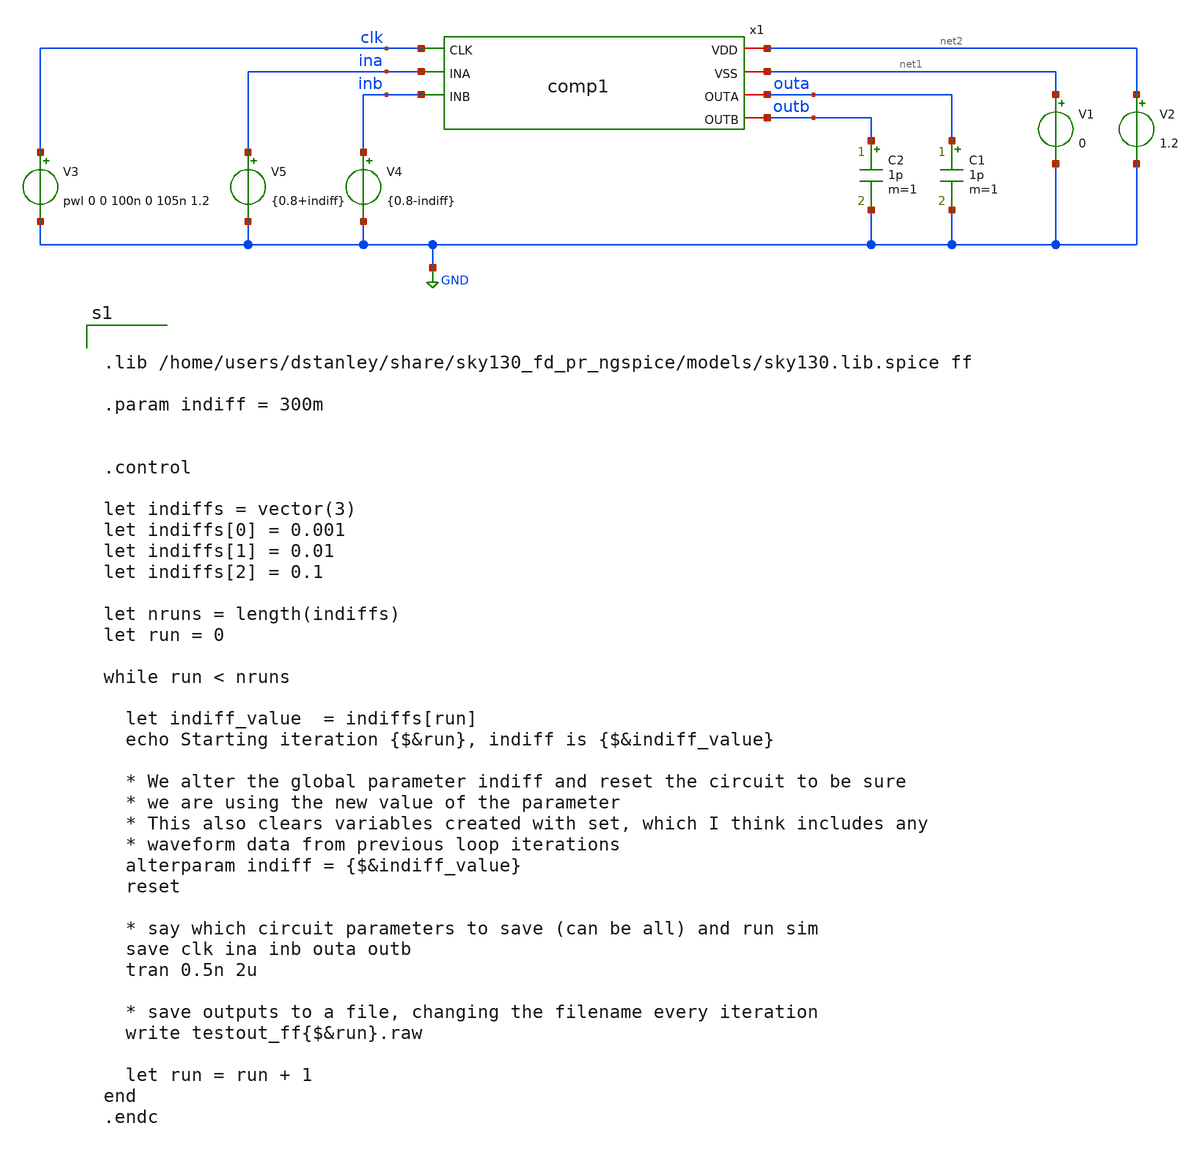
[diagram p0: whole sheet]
** sch_path: comp1_loop_test_ff.sch
**.subckt comp1_loop_test_ff
x1 net2 net1 clk ina inb outa outb comp1
V1 net1 GND 0
V2 net2 GND 1.2
C1 outa GND 1p m=1
C2 outb GND 1p m=1
V3 clk GND pwl 0 0 100n 0 105n 1.2
V4 inb GND {0.8-indiff}
V5 ina GND {0.8+indiff}
**** begin user architecture code


.lib /home/users/dstanley/share/sky130_fd_pr_ngspice/models/sky130.lib.spice ff

.param indiff = 300m


.control

let indiffs = vector(3)
let indiffs[0] = 0.001
let indiffs[1] = 0.01
let indiffs[2] = 0.1

let nruns = length(indiffs)
let run = 0

while run < nruns

  let indiff_value  = indiffs[run]
  echo Starting iteration {$&run}, indiff is {$&indiff_value}

  * We alter the global parameter indiff and reset the circuit to be sure
  * we are using the new value of the parameter
  * This also clears variables created with set, which I think includes any
  * waveform data from previous loop iterations
  alterparam indiff = {$&indiff_value}
  reset

  * say which circuit parameters to save (can be all) and run sim
  save clk ina inb outa outb
  tran 0.5n 2u

  * save outputs to a file, changing the filename every iteration
  write testout_ff{$&run}.raw

  let run = run + 1
end
.endc


**** end user architecture code
**.ends

* expanding   symbol:  /home/users/dstanley/EE272B/xschem_tests/comp1.sym # of pins=7
** sym_path: comp1.sym
** sch_path: comp1.sch
.subckt comp1 VDD VSS CLK INA INB OUTA OUTB
*.iopin VSS
*.iopin VDD
*.iopin OUTB
*.iopin OUTA
*.ipin INB
*.ipin INA
*.ipin CLK
XM1 net2 CLK VSS VSS sky130_fd_pr__nfet_01v8 L=0.15 W=1 nf=1 ad='int((nf+1)/2) * W/nf * 0.29' as='int((nf+2)/2) * W/nf * 0.29'
+ pd='2*int((nf+1)/2) * (W/nf + 0.29)' ps='2*int((nf+2)/2) * (W/nf + 0.29)' nrd='0.29 / W' nrs='0.29 / W'
+ sa=0 sb=0 sd=0 mult=1 m=1
XM2 net1 INA net2 VSS sky130_fd_pr__nfet_01v8 L=0.15 W=1 nf=1 ad='int((nf+1)/2) * W/nf * 0.29' as='int((nf+2)/2) * W/nf * 0.29'
+ pd='2*int((nf+1)/2) * (W/nf + 0.29)' ps='2*int((nf+2)/2) * (W/nf + 0.29)' nrd='0.29 / W' nrs='0.29 / W'
+ sa=0 sb=0 sd=0 mult=1 m=1
XM4 OUTB OUTA net1 VSS sky130_fd_pr__nfet_01v8 L=0.15 W=1 nf=1 ad='int((nf+1)/2) * W/nf * 0.29' as='int((nf+2)/2) * W/nf * 0.29'
+ pd='2*int((nf+1)/2) * (W/nf + 0.29)' ps='2*int((nf+2)/2) * (W/nf + 0.29)' nrd='0.29 / W' nrs='0.29 / W'
+ sa=0 sb=0 sd=0 mult=1 m=1
XM5 OUTB OUTA VDD VDD sky130_fd_pr__pfet_01v8 L=0.15 W=1 nf=1 ad='int((nf+1)/2) * W/nf * 0.29' as='int((nf+2)/2) * W/nf * 0.29'
+ pd='2*int((nf+1)/2) * (W/nf + 0.29)' ps='2*int((nf+2)/2) * (W/nf + 0.29)' nrd='0.29 / W' nrs='0.29 / W'
+ sa=0 sb=0 sd=0 mult=1 m=1
XM6 OUTB CLK VDD VDD sky130_fd_pr__pfet_01v8 L=0.15 W=1 nf=1 ad='int((nf+1)/2) * W/nf * 0.29' as='int((nf+2)/2) * W/nf * 0.29'
+ pd='2*int((nf+1)/2) * (W/nf + 0.29)' ps='2*int((nf+2)/2) * (W/nf + 0.29)' nrd='0.29 / W' nrs='0.29 / W'
+ sa=0 sb=0 sd=0 mult=1 m=1
XM3 net3 INB net2 VSS sky130_fd_pr__nfet_01v8 L=0.15 W=1 nf=1 ad='int((nf+1)/2) * W/nf * 0.29' as='int((nf+2)/2) * W/nf * 0.29'
+ pd='2*int((nf+1)/2) * (W/nf + 0.29)' ps='2*int((nf+2)/2) * (W/nf + 0.29)' nrd='0.29 / W' nrs='0.29 / W'
+ sa=0 sb=0 sd=0 mult=1 m=1
XM7 OUTA OUTB net3 VSS sky130_fd_pr__nfet_01v8 L=0.15 W=1 nf=1 ad='int((nf+1)/2) * W/nf * 0.29' as='int((nf+2)/2) * W/nf * 0.29'
+ pd='2*int((nf+1)/2) * (W/nf + 0.29)' ps='2*int((nf+2)/2) * (W/nf + 0.29)' nrd='0.29 / W' nrs='0.29 / W'
+ sa=0 sb=0 sd=0 mult=1 m=1
XM8 OUTA OUTB VDD VDD sky130_fd_pr__pfet_01v8 L=0.15 W=1 nf=1 ad='int((nf+1)/2) * W/nf * 0.29' as='int((nf+2)/2) * W/nf * 0.29'
+ pd='2*int((nf+1)/2) * (W/nf + 0.29)' ps='2*int((nf+2)/2) * (W/nf + 0.29)' nrd='0.29 / W' nrs='0.29 / W'
+ sa=0 sb=0 sd=0 mult=1 m=1
XM9 OUTA CLK VDD VDD sky130_fd_pr__pfet_01v8 L=0.15 W=1 nf=1 ad='int((nf+1)/2) * W/nf * 0.29' as='int((nf+2)/2) * W/nf * 0.29'
+ pd='2*int((nf+1)/2) * (W/nf + 0.29)' ps='2*int((nf+2)/2) * (W/nf + 0.29)' nrd='0.29 / W' nrs='0.29 / W'
+ sa=0 sb=0 sd=0 mult=1 m=1
.ends

.GLOBAL GND
.end
